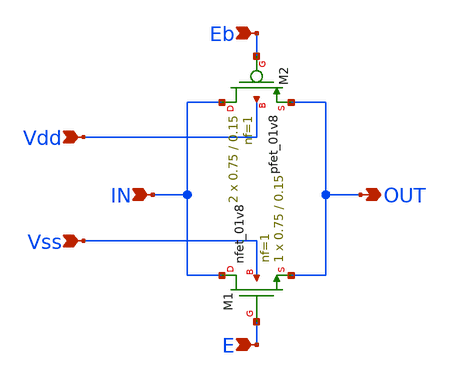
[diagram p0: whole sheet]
** sch_path: icdesign/sch/TGate/tgate.sch
**.subckt tgate OUT IN Eb E Vdd Vss
*.opin OUT
*.ipin IN
*.ipin Eb
*.ipin E
*.ipin Vdd
*.ipin Vss
XM1 IN E OUT Vss sky130_fd_pr__nfet_01v8 L=0.15 W=0.75 nf=1 ad='int((nf+1)/2) * W/nf * 0.29' as='int((nf+2)/2) * W/nf * 0.29'
+ pd='2*int((nf+1)/2) * (W/nf + 0.29)' ps='2*int((nf+2)/2) * (W/nf + 0.29)' nrd='0.29 / W' nrs='0.29 / W'
+ sa=0 sb=0 sd=0 mult=1 m=1
XM2 IN Eb OUT Vdd sky130_fd_pr__pfet_01v8 L=0.15 W=0.75 nf=1 ad='int((nf+1)/2) * W/nf * 0.29' as='int((nf+2)/2) * W/nf * 0.29'
+ pd='2*int((nf+1)/2) * (W/nf + 0.29)' ps='2*int((nf+2)/2) * (W/nf + 0.29)' nrd='0.29 / W' nrs='0.29 / W'
+ sa=0 sb=0 sd=0 mult=2 m=2
**.ends
.end
